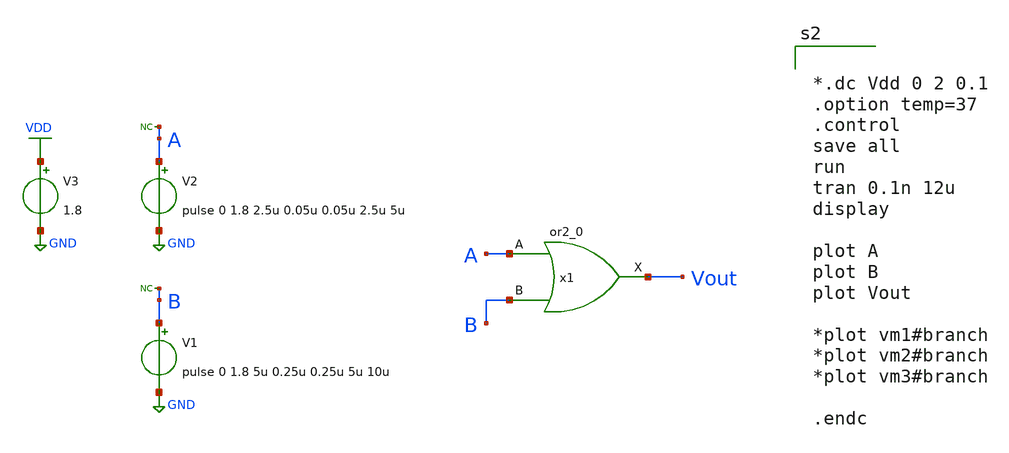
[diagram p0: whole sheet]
** sch_path: xschem/ip_block/logic_gate/tb_or.sch
**.subckt tb_or
V1 B GND pulse 0 1.8 5u 0.25u 0.25u 5u 10u
* noconn B
V2 A GND pulse 0 1.8 2.5u 0.05u 0.05u 2.5u 5u
* noconn A
V3 VDD GND 1.8
x1 A B VGND VNB VPB VPWR Vout sky130_fd_sc_hd__or2_0
**** begin user architecture code

** opencircuitdesign pdks install
.lib $::SKYWATER_MODELS/sky130.lib.spice tt




*.dc Vdd 0 2 0.1
.option temp=37
.control
save all
run
tran 0.1n 12u
display

plot A
plot B
plot Vout

*plot vm1#branch
*plot vm2#branch
*plot vm3#branch

.endc


**** end user architecture code
**.ends
.GLOBAL GND
.GLOBAL VDD
.end
